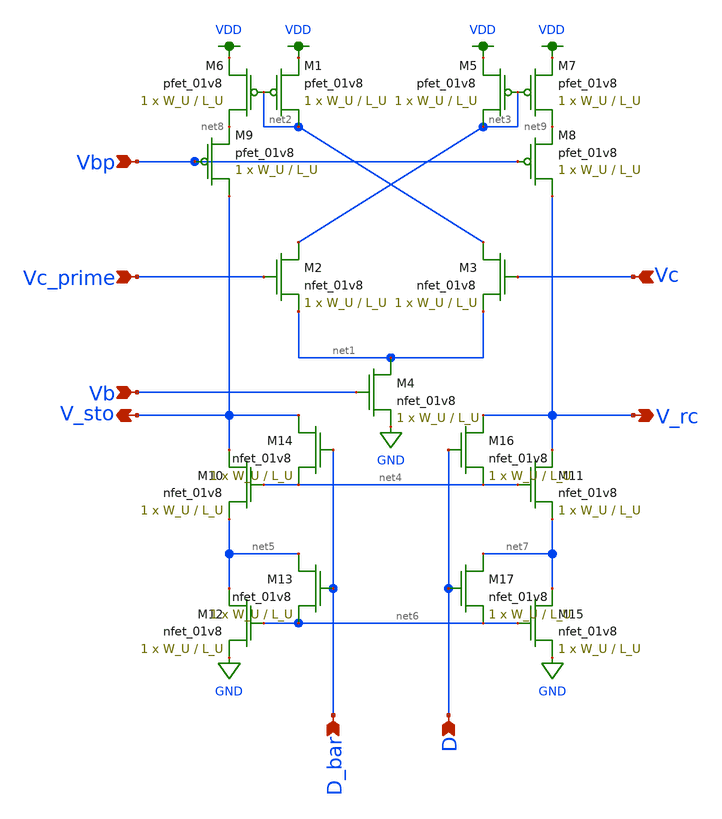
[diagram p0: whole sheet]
** sch_path: schematics/OTA_minus.sch
**.subckt OTA_minus Vbp Vb D_bar D Vc_prime Vc V_rc V_sto
*.ipin Vbp
*.ipin Vb
*.ipin D_bar
*.ipin D
*.ipin Vc_prime
*.ipin Vc
*.opin V_rc
*.opin V_sto
XM1 net2 net2 VDD VDD sky130_fd_pr__pfet_01v8 L=L_U W=W_U nf=1 ad='int((nf+1)/2) * W/nf * 0.29' as='int((nf+2)/2) * W/nf * 0.29'
+ pd='2*int((nf+1)/2) * (W/nf + 0.29)' ps='2*int((nf+2)/2) * (W/nf + 0.29)' nrd='0.29 / W' nrs='0.29 / W'
+ sa=0 sb=0 sd=0 mult=1 m=1
XM2 net3 Vc_prime net1 GND sky130_fd_pr__nfet_01v8 L=L_U W=W_U nf=1 ad='int((nf+1)/2) * W/nf * 0.29'
+ as='int((nf+2)/2) * W/nf * 0.29' pd='2*int((nf+1)/2) * (W/nf + 0.29)' ps='2*int((nf+2)/2) * (W/nf + 0.29)'
+ nrd='0.29 / W' nrs='0.29 / W' sa=0 sb=0 sd=0 mult=1 m=1
XM3 net2 Vc net1 GND sky130_fd_pr__nfet_01v8 L=L_U W=W_U nf=1 ad='int((nf+1)/2) * W/nf * 0.29' as='int((nf+2)/2) * W/nf * 0.29'
+ pd='2*int((nf+1)/2) * (W/nf + 0.29)' ps='2*int((nf+2)/2) * (W/nf + 0.29)' nrd='0.29 / W' nrs='0.29 / W'
+ sa=0 sb=0 sd=0 mult=1 m=1
XM4 net1 Vb GND GND sky130_fd_pr__nfet_01v8 L=L_U W=W_U nf=1 ad='int((nf+1)/2) * W/nf * 0.29' as='int((nf+2)/2) * W/nf * 0.29'
+ pd='2*int((nf+1)/2) * (W/nf + 0.29)' ps='2*int((nf+2)/2) * (W/nf + 0.29)' nrd='0.29 / W' nrs='0.29 / W'
+ sa=0 sb=0 sd=0 mult=1 m=1
XM5 net3 net3 VDD VDD sky130_fd_pr__pfet_01v8 L=L_U W=W_U nf=1 ad='int((nf+1)/2) * W/nf * 0.29' as='int((nf+2)/2) * W/nf * 0.29'
+ pd='2*int((nf+1)/2) * (W/nf + 0.29)' ps='2*int((nf+2)/2) * (W/nf + 0.29)' nrd='0.29 / W' nrs='0.29 / W'
+ sa=0 sb=0 sd=0 mult=1 m=1
XM6 net8 net2 VDD VDD sky130_fd_pr__pfet_01v8 L=L_U W=W_U nf=1 ad='int((nf+1)/2) * W/nf * 0.29' as='int((nf+2)/2) * W/nf * 0.29'
+ pd='2*int((nf+1)/2) * (W/nf + 0.29)' ps='2*int((nf+2)/2) * (W/nf + 0.29)' nrd='0.29 / W' nrs='0.29 / W'
+ sa=0 sb=0 sd=0 mult=1 m=1
XM7 net9 net3 VDD VDD sky130_fd_pr__pfet_01v8 L=L_U W=W_U nf=1 ad='int((nf+1)/2) * W/nf * 0.29' as='int((nf+2)/2) * W/nf * 0.29'
+ pd='2*int((nf+1)/2) * (W/nf + 0.29)' ps='2*int((nf+2)/2) * (W/nf + 0.29)' nrd='0.29 / W' nrs='0.29 / W'
+ sa=0 sb=0 sd=0 mult=1 m=1
XM8 V_rc Vbp net9 VDD sky130_fd_pr__pfet_01v8 L=L_U W=W_U nf=1 ad='int((nf+1)/2) * W/nf * 0.29' as='int((nf+2)/2) * W/nf * 0.29'
+ pd='2*int((nf+1)/2) * (W/nf + 0.29)' ps='2*int((nf+2)/2) * (W/nf + 0.29)' nrd='0.29 / W' nrs='0.29 / W'
+ sa=0 sb=0 sd=0 mult=1 m=1
XM9 V_sto Vbp net8 VDD sky130_fd_pr__pfet_01v8 L=L_U W=W_U nf=1 ad='int((nf+1)/2) * W/nf * 0.29' as='int((nf+2)/2) * W/nf * 0.29'
+ pd='2*int((nf+1)/2) * (W/nf + 0.29)' ps='2*int((nf+2)/2) * (W/nf + 0.29)' nrd='0.29 / W' nrs='0.29 / W'
+ sa=0 sb=0 sd=0 mult=1 m=1
XM10 V_sto net4 net5 GND sky130_fd_pr__nfet_01v8 L=L_U W=W_U nf=1 ad='int((nf+1)/2) * W/nf * 0.29' as='int((nf+2)/2) * W/nf * 0.29'
+ pd='2*int((nf+1)/2) * (W/nf + 0.29)' ps='2*int((nf+2)/2) * (W/nf + 0.29)' nrd='0.29 / W' nrs='0.29 / W'
+ sa=0 sb=0 sd=0 mult=1 m=1
XM11 V_rc net4 net7 GND sky130_fd_pr__nfet_01v8 L=L_U W=W_U nf=1 ad='int((nf+1)/2) * W/nf * 0.29' as='int((nf+2)/2) * W/nf * 0.29'
+ pd='2*int((nf+1)/2) * (W/nf + 0.29)' ps='2*int((nf+2)/2) * (W/nf + 0.29)' nrd='0.29 / W' nrs='0.29 / W'
+ sa=0 sb=0 sd=0 mult=1 m=1
XM12 net5 net6 GND GND sky130_fd_pr__nfet_01v8 L=L_U W=W_U nf=1 ad='int((nf+1)/2) * W/nf * 0.29' as='int((nf+2)/2) * W/nf * 0.29'
+ pd='2*int((nf+1)/2) * (W/nf + 0.29)' ps='2*int((nf+2)/2) * (W/nf + 0.29)' nrd='0.29 / W' nrs='0.29 / W'
+ sa=0 sb=0 sd=0 mult=1 m=1
XM13 net5 D_bar net6 GND sky130_fd_pr__nfet_01v8 L=L_U W=W_U nf=1 ad='int((nf+1)/2) * W/nf * 0.29' as='int((nf+2)/2) * W/nf * 0.29'
+ pd='2*int((nf+1)/2) * (W/nf + 0.29)' ps='2*int((nf+2)/2) * (W/nf + 0.29)' nrd='0.29 / W' nrs='0.29 / W'
+ sa=0 sb=0 sd=0 mult=1 m=1
XM14 V_sto D_bar net4 GND sky130_fd_pr__nfet_01v8 L=L_U W=W_U nf=1 ad='int((nf+1)/2) * W/nf * 0.29' as='int((nf+2)/2) * W/nf * 0.29'
+ pd='2*int((nf+1)/2) * (W/nf + 0.29)' ps='2*int((nf+2)/2) * (W/nf + 0.29)' nrd='0.29 / W' nrs='0.29 / W'
+ sa=0 sb=0 sd=0 mult=1 m=1
XM15 net7 net6 GND GND sky130_fd_pr__nfet_01v8 L=L_U W=W_U nf=1 ad='int((nf+1)/2) * W/nf * 0.29' as='int((nf+2)/2) * W/nf * 0.29'
+ pd='2*int((nf+1)/2) * (W/nf + 0.29)' ps='2*int((nf+2)/2) * (W/nf + 0.29)' nrd='0.29 / W' nrs='0.29 / W'
+ sa=0 sb=0 sd=0 mult=1 m=1
XM16 V_rc D net4 GND sky130_fd_pr__nfet_01v8 L=L_U W=W_U nf=1 ad='int((nf+1)/2) * W/nf * 0.29' as='int((nf+2)/2) * W/nf * 0.29'
+ pd='2*int((nf+1)/2) * (W/nf + 0.29)' ps='2*int((nf+2)/2) * (W/nf + 0.29)' nrd='0.29 / W' nrs='0.29 / W'
+ sa=0 sb=0 sd=0 mult=1 m=1
XM17 net7 D net6 GND sky130_fd_pr__nfet_01v8 L=L_U W=W_U nf=1 ad='int((nf+1)/2) * W/nf * 0.29' as='int((nf+2)/2) * W/nf * 0.29'
+ pd='2*int((nf+1)/2) * (W/nf + 0.29)' ps='2*int((nf+2)/2) * (W/nf + 0.29)' nrd='0.29 / W' nrs='0.29 / W'
+ sa=0 sb=0 sd=0 mult=1 m=1
**.ends
.GLOBAL VDD
.GLOBAL GND
.end
